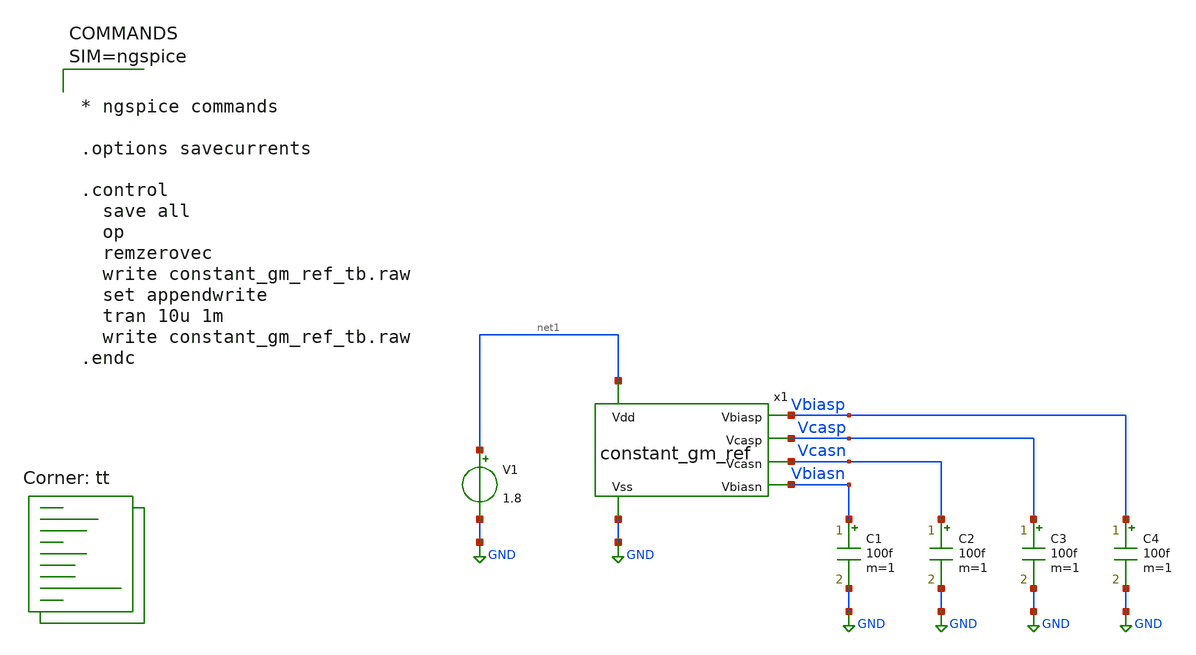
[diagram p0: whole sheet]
** sch_path: testbench/constant_gm_ref_tb.sch
**.subckt constant_gm_ref_tb
x1 net1 Vcasp Vbiasp Vcasn Vbiasn GND constant_gm_ref
V1 net1 GND 1.8
C1 Vbiasn GND 100f m=1
C2 Vcasn GND 100f m=1
C3 Vcasp GND 100f m=1
C4 Vbiasp GND 100f m=1
**** begin user architecture code
.lib $::SKYWATER_MODELS/sky130.lib.spice tt



* ngspice commands

.options savecurrents

.control
  save all
  op
  remzerovec
  write constant_gm_ref_tb.raw
  set appendwrite
  tran 10u 1m
  write constant_gm_ref_tb.raw
.endc



**** end user architecture code
**.ends

* expanding   symbol:  /foss/designs/ota_1g/schematic/constant_gm_ref.sym # of pins=6
** sym_path: schematic/constant_gm_ref.sym
** sch_path: schematic/constant_gm_ref.sch
.subckt constant_gm_ref Vdd Vcasp Vbiasp Vcasn Vbiasn Vss
*.ipin Vdd
*.ipin Vss
*.opin Vcasn
*.opin Vbiasn
*.opin Vcasp
*.opin Vbiasp
XM2 Vcasp Vbiasn Vss Vss sky130_fd_pr__nfet_01v8 L=0.3 W=5 nf=1 ad='int((1 + 1)/2) * 5 / 1 * 0.29' as='int((1 + 2)/2) * 5 / 1 * 0.29'
+ pd='2*int((1 + 1)/2) * (5 / 1 + 0.29)' ps='2*int((1 + 2)/2) * (5 / 1 + 0.29)' nrd='0.29 / 5 ' nrs='0.29 / 5 '
+ sa=0 sb=0 sd=0 mult=1 m=1
XM1 net2 Vbiasn Vss Vss sky130_fd_pr__nfet_01v8 L=0.3 W=5 nf=1 ad='int((1 + 1)/2) * 5 / 1 * 0.29' as='int((1 + 2)/2) * 5 / 1 * 0.29'
+ pd='2*int((1 + 1)/2) * (5 / 1 + 0.29)' ps='2*int((1 + 2)/2) * (5 / 1 + 0.29)' nrd='0.29 / 5 ' nrs='0.29 / 5 '
+ sa=0 sb=0 sd=0 mult=1 m=1
XM11 Vcasp Vcasp Vdd Vdd sky130_fd_pr__pfet_01v8 L=0.3 W=2 nf=1 ad='int((nf+1)/2) * W/nf * 0.29' as='int((nf+2)/2) * W/nf * 0.29'
+ pd='2*int((nf+1)/2) * (W/nf + 0.29)' ps='2*int((nf+2)/2) * (W/nf + 0.29)' nrd='0.29 / W' nrs='0.29 / W'
+ sa=0 sb=0 sd=0 mult=1 m=1
XM3 net2 Vcasp net1 net1 sky130_fd_pr__pfet_01v8 L=0.3 W=8 nf=1 ad='int((nf+1)/2) * W/nf * 0.29' as='int((nf+2)/2) * W/nf * 0.29'
+ pd='2*int((nf+1)/2) * (W/nf + 0.29)' ps='2*int((nf+2)/2) * (W/nf + 0.29)' nrd='0.29 / W' nrs='0.29 / W'
+ sa=0 sb=0 sd=0 mult=1 m=1
XR9 net1 Vdd Vdd sky130_fd_pr__res_xhigh_po W=1 L=10 mult=1 m=1
XM4 net4 Vbiasn Vss Vss sky130_fd_pr__nfet_01v8 L=0.3 W=1 nf=1 ad='int((1 + 1)/2) * 1 / 1 * 0.29' as='int((1 + 2)/2) * 1 / 1 * 0.29'
+ pd='2*int((1 + 1)/2) * (1 / 1 + 0.29)' ps='2*int((1 + 2)/2) * (1 / 1 + 0.29)' nrd='0.29 / 1 ' nrs='0.29 / 1 '
+ sa=0 sb=0 sd=0 mult=1 m=1
XM5 Vbiasp Vcasp net3 Vdd sky130_fd_pr__pfet_01v8 L=0.3 W=2 nf=1 ad='int((nf+1)/2) * W/nf * 0.29' as='int((nf+2)/2) * W/nf * 0.29'
+ pd='2*int((nf+1)/2) * (W/nf + 0.29)' ps='2*int((nf+2)/2) * (W/nf + 0.29)' nrd='0.29 / W' nrs='0.29 / W'
+ sa=0 sb=0 sd=0 mult=1 m=1
XM6 net3 Vbiasp Vdd Vdd sky130_fd_pr__pfet_01v8 L=0.3 W=2 nf=1 ad='int((nf+1)/2) * W/nf * 0.29' as='int((nf+2)/2) * W/nf * 0.29'
+ pd='2*int((nf+1)/2) * (W/nf + 0.29)' ps='2*int((nf+2)/2) * (W/nf + 0.29)' nrd='0.29 / W' nrs='0.29 / W'
+ sa=0 sb=0 sd=0 mult=1 m=1
XM7 Vbiasp Vcasn net4 Vss sky130_fd_pr__nfet_01v8 L=0.3 W=1 nf=1 ad='int((1 + 1)/2) * 1 / 1 * 0.29' as='int((1 + 2)/2) * 1 / 1 * 0.29'
+ pd='2*int((1 + 1)/2) * (1 / 1 + 0.29)' ps='2*int((1 + 2)/2) * (1 / 1 + 0.29)' nrd='0.29 / 1 ' nrs='0.29 / 1 '
+ sa=0 sb=0 sd=0 mult=1 m=1
XM8 Vcasn Vcasp net5 Vdd sky130_fd_pr__pfet_01v8 L=0.3 W=10 nf=1 ad='int((nf+1)/2) * W/nf * 0.29' as='int((nf+2)/2) * W/nf * 0.29'
+ pd='2*int((nf+1)/2) * (W/nf + 0.29)' ps='2*int((nf+2)/2) * (W/nf + 0.29)' nrd='0.29 / W' nrs='0.29 / W'
+ sa=0 sb=0 sd=0 mult=1 m=1
XM9 net5 Vbiasp Vdd Vdd sky130_fd_pr__pfet_01v8 L=0.3 W=10 nf=1 ad='int((nf+1)/2) * W/nf * 0.29' as='int((nf+2)/2) * W/nf * 0.29'
+ pd='2*int((nf+1)/2) * (W/nf + 0.29)' ps='2*int((nf+2)/2) * (W/nf + 0.29)' nrd='0.29 / W' nrs='0.29 / W'
+ sa=0 sb=0 sd=0 mult=1 m=1
XM10 Vcasn Vcasn Vss Vss sky130_fd_pr__nfet_01v8 L=0.3 W=1 nf=1 ad='int((1 + 1)/2) * 1 / 1 * 0.29' as='int((1 + 2)/2) * 1 / 1 * 0.29'
+ pd='2*int((1 + 1)/2) * (1 / 1 + 0.29)' ps='2*int((1 + 2)/2) * (1 / 1 + 0.29)' nrd='0.29 / 1 ' nrs='0.29 / 1 '
+ sa=0 sb=0 sd=0 mult=1 m=1
XM14 net6 Vcasp Vdd Vdd sky130_fd_pr__pfet_01v8 L=0.3 W=1 nf=1 ad='int((nf+1)/2) * W/nf * 0.29' as='int((nf+2)/2) * W/nf * 0.29'
+ pd='2*int((nf+1)/2) * (W/nf + 0.29)' ps='2*int((nf+2)/2) * (W/nf + 0.29)' nrd='0.29 / W' nrs='0.29 / W'
+ sa=0 sb=0 sd=0 mult=1 m=1
XM15 net6 Vdd Vss Vss sky130_fd_pr__nfet_01v8 L=0.3 W=1 nf=1 ad='int((1 + 1)/2) * 1 / 1 * 0.29' as='int((1 + 2)/2) * 1 / 1 * 0.29'
+ pd='2*int((1 + 1)/2) * (1 / 1 + 0.29)' ps='2*int((1 + 2)/2) * (1 / 1 + 0.29)' nrd='0.29 / 1 ' nrs='0.29 / 1 '
+ sa=0 sb=0 sd=0 mult=1 m=1
x1 Vdd Vbiasn Vcasp net2 Vss ota_n_selfbias
XM12 net7 net6 Vdd Vdd sky130_fd_pr__pfet_01v8 L=0.3 W=1 nf=1 ad='int((nf+1)/2) * W/nf * 0.29' as='int((nf+2)/2) * W/nf * 0.29'
+ pd='2*int((nf+1)/2) * (W/nf + 0.29)' ps='2*int((nf+2)/2) * (W/nf + 0.29)' nrd='0.29 / W' nrs='0.29 / W'
+ sa=0 sb=0 sd=0 mult=1 m=1
XM13 net8 net6 Vdd Vdd sky130_fd_pr__pfet_01v8 L=0.3 W=1 nf=1 ad='int((nf+1)/2) * W/nf * 0.29' as='int((nf+2)/2) * W/nf * 0.29'
+ pd='2*int((nf+1)/2) * (W/nf + 0.29)' ps='2*int((nf+2)/2) * (W/nf + 0.29)' nrd='0.29 / W' nrs='0.29 / W'
+ sa=0 sb=0 sd=0 mult=1 m=1
XC1 Vbiasn Vss sky130_fd_pr__cap_mim_m3_1 W=10 L=10 MF=1 m=1
.ends


* expanding   symbol:  /foss/designs/ota_1g/schematic/ota_n_selfbias.sym # of pins=5
** sym_path: schematic/ota_n_selfbias.sym
** sch_path: schematic/ota_n_selfbias.sch
.subckt ota_n_selfbias Vdd Vout Vim Vip Vss
*.ipin Vim
*.ipin Vip
*.opin Vout
*.ipin Vdd
*.ipin Vss
XM1 net1 Vim net3 Vss sky130_fd_pr__nfet_01v8_lvt L=0.4 W=1 nf=1 ad='int((1 + 1)/2) * 1 / 1 * 0.29' as='int((1 + 2)/2) * 1 / 1 * 0.29'
+ pd='2*int((1 + 1)/2) * (1 / 1 + 0.29)' ps='2*int((1 + 2)/2) * (1 / 1 + 0.29)' nrd='0.29 / 1 ' nrs='0.29 / 1 '
+ sa=0 sb=0 sd=0 mult=1 m=1
XM2 net2 Vip net3 Vss sky130_fd_pr__nfet_01v8_lvt L=0.4 W=1 nf=1 ad='int((1 + 1)/2) * 1 / 1 * 0.29' as='int((1 + 2)/2) * 1 / 1 * 0.29'
+ pd='2*int((1 + 1)/2) * (1 / 1 + 0.29)' ps='2*int((1 + 2)/2) * (1 / 1 + 0.29)' nrd='0.29 / 1 ' nrs='0.29 / 1 '
+ sa=0 sb=0 sd=0 mult=1 m=1
XM3 net3 net5 Vss Vss sky130_fd_pr__nfet_01v8_lvt L=0.4 W=1 nf=1 ad='int((1 + 1)/2) * 1 / 1 * 0.29' as='int((1 + 2)/2) * 1 / 1 * 0.29'
+ pd='2*int((1 + 1)/2) * (1 / 1 + 0.29)' ps='2*int((1 + 2)/2) * (1 / 1 + 0.29)' nrd='0.29 / 1 ' nrs='0.29 / 1 '
+ sa=0 sb=0 sd=0 mult=1 m=1
XM10 Vout net2 Vdd Vdd sky130_fd_pr__pfet_01v8_lvt L=0.4 W=1 nf=1 ad='int((1 + 1)/2) * 1 / 1 * 0.29'
+ as='int((1 + 2)/2) * 1 / 1 * 0.29' pd='2*int((1 + 1)/2) * (1 / 1 + 0.29)' ps='2*int((1 + 2)/2) * (1 / 1 + 0.29)'
+ nrd='0.29 / 1 ' nrs='0.29 / 1 ' sa=0 sb=0 sd=0 mult=1 m=1
XM4 net2 net2 Vdd Vdd sky130_fd_pr__pfet_01v8_lvt L=0.4 W=1 nf=1 ad='int((1 + 1)/2) * 1 / 1 * 0.29' as='int((1 + 2)/2) * 1 / 1 * 0.29'
+ pd='2*int((1 + 1)/2) * (1 / 1 + 0.29)' ps='2*int((1 + 2)/2) * (1 / 1 + 0.29)' nrd='0.29 / 1 ' nrs='0.29 / 1 '
+ sa=0 sb=0 sd=0 mult=1 m=1
XM5 net1 net1 Vdd Vdd sky130_fd_pr__pfet_01v8_lvt L=0.4 W=1 nf=1 ad='int((1 + 1)/2) * 1 / 1 * 0.29' as='int((1 + 2)/2) * 1 / 1 * 0.29'
+ pd='2*int((1 + 1)/2) * (1 / 1 + 0.29)' ps='2*int((1 + 2)/2) * (1 / 1 + 0.29)' nrd='0.29 / 1 ' nrs='0.29 / 1 '
+ sa=0 sb=0 sd=0 mult=1 m=1
XM7 net4 net1 Vdd Vdd sky130_fd_pr__pfet_01v8_lvt L=0.4 W=1 nf=1 ad='int((1 + 1)/2) * 1 / 1 * 0.29' as='int((1 + 2)/2) * 1 / 1 * 0.29'
+ pd='2*int((1 + 1)/2) * (1 / 1 + 0.29)' ps='2*int((1 + 2)/2) * (1 / 1 + 0.29)' nrd='0.29 / 1 ' nrs='0.29 / 1 '
+ sa=0 sb=0 sd=0 mult=1 m=1
XM6 net4 net4 Vss Vss sky130_fd_pr__nfet_01v8_lvt L=0.4 W=1 nf=1 ad='int((1 + 1)/2) * 1 / 1 * 0.29' as='int((1 + 2)/2) * 1 / 1 * 0.29'
+ pd='2*int((1 + 1)/2) * (1 / 1 + 0.29)' ps='2*int((1 + 2)/2) * (1 / 1 + 0.29)' nrd='0.29 / 1 ' nrs='0.29 / 1 '
+ sa=0 sb=0 sd=0 mult=1 m=1
XM8 Vout net4 Vss Vss sky130_fd_pr__nfet_01v8_lvt L=0.4 W=1 nf=1 ad='int((1 + 1)/2) * 1 / 1 * 0.29' as='int((1 + 2)/2) * 1 / 1 * 0.29'
+ pd='2*int((1 + 1)/2) * (1 / 1 + 0.29)' ps='2*int((1 + 2)/2) * (1 / 1 + 0.29)' nrd='0.29 / 1 ' nrs='0.29 / 1 '
+ sa=0 sb=0 sd=0 mult=1 m=1
XM9 net5 net5 Vss Vss sky130_fd_pr__nfet_01v8_lvt L=0.4 W=1 nf=1 ad='int((1 + 1)/2) * 1 / 1 * 0.29' as='int((1 + 2)/2) * 1 / 1 * 0.29'
+ pd='2*int((1 + 1)/2) * (1 / 1 + 0.29)' ps='2*int((1 + 2)/2) * (1 / 1 + 0.29)' nrd='0.29 / 1 ' nrs='0.29 / 1 '
+ sa=0 sb=0 sd=0 mult=1 m=1
XR9 net5 Vdd Vss sky130_fd_pr__res_xhigh_po W=1 L=10 mult=1 m=1
.ends

.GLOBAL GND
.end
